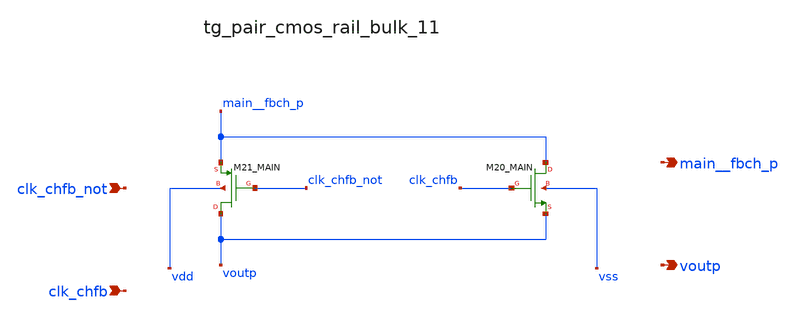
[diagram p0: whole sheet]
** sch_path: analog-db/raw/ia_004_fan_chopper_rrl/hier/blocks/tg_pair_cmos_rail_bulk_11.sch
**.subckt tg_pair_cmos_rail_bulk_11 clk_chfb_not clk_chfb main__fbch_p voutp
*.ipin clk_chfb_not
*.ipin clk_chfb
*.opin main__fbch_p
*.opin voutp
XM20_MAIN main__fbch_p clk_chfb voutp vss sg13_lv_nmos w=x_dut_xm20_main_w l=x_dut_xm20_main_l ng=1
+ m=x_dut_xm20_main_m
XM21_MAIN voutp clk_chfb_not main__fbch_p vdd sg13_lv_pmos w=x_dut_xm21_main_w l=x_dut_xm21_main_l
+ ng=1 m=x_dut_xm21_main_m
**.ends
.end
